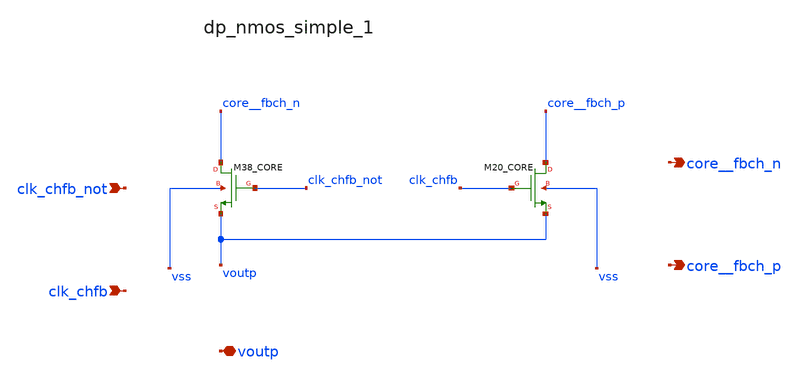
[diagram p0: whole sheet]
** sch_path: analog-db/raw/ia_006_fan_chopper_cmfb/hier/blocks/dp_nmos_simple_1.sch
**.subckt dp_nmos_simple_1 clk_chfb_not clk_chfb voutp core__fbch_n core__fbch_p
*.ipin clk_chfb_not
*.ipin clk_chfb
*.iopin voutp
*.opin core__fbch_n
*.opin core__fbch_p
XM20_CORE core__fbch_p clk_chfb voutp vss sg13_lv_nmos w=x_dut_xm20_core_w l=x_dut_xm20_core_l ng=1
+ m=x_dut_xm20_core_m
XM38_CORE core__fbch_n clk_chfb_not voutp vss sg13_lv_nmos w=x_dut_xm38_core_w l=x_dut_xm38_core_l
+ ng=1 m=x_dut_xm38_core_m
**.ends
.end
